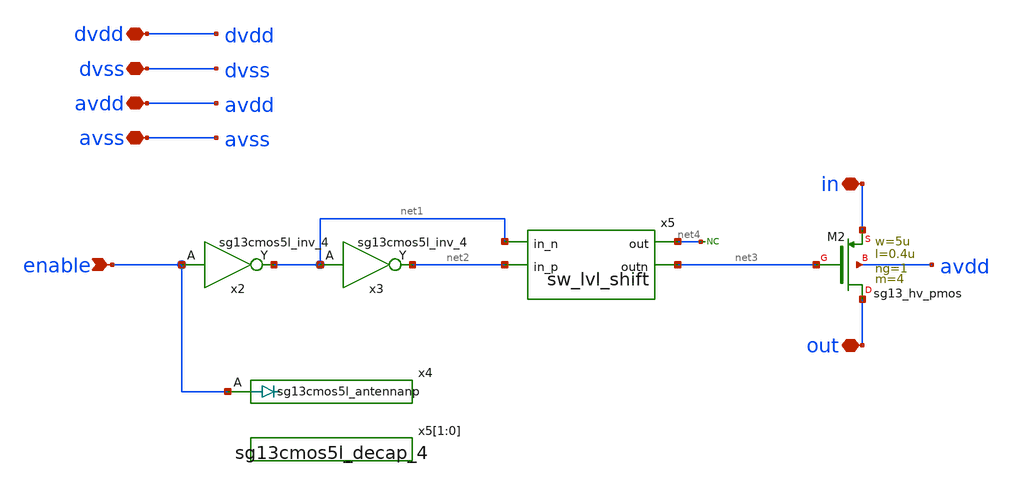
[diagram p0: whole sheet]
** sch_path: macros/ocd_analog_switches/schematic/xschem/analog_pswitch_small.sch
**.subckt analog_pswitch_small in out enable dvdd dvss avdd avss
*.iopin in
*.iopin out
*.ipin enable
*.iopin dvdd
*.iopin dvss
*.iopin avdd
*.iopin avss
XM2 out net3 in avdd sg13_hv_pmos w=5u l=0.4u ng=1 m=4 mm_ok=1
x2 net1 enable dvdd dvss sg13cmos5l_inv_4
x3 net2 net1 dvdd dvss sg13cmos5l_inv_4
x4 enable dvdd dvss sg13cmos5l_antennanp
x5[1] dvdd dvss sg13cmos5l_decap_4
x5[0] dvdd dvss sg13cmos5l_decap_4
x5 net2 net1 net4 net3 avdd avss sw_lvl_shift
* noconn #net4
**.ends

* expanding   symbol:  sw_lvl_shift.sym # of pins=4
** sym_path: macros/ocd_analog_switches/schematic/xschem/sw_lvl_shift.sym
** sch_path: macros/ocd_analog_switches/schematic/xschem/sw_lvl_shift.sch
.subckt sw_lvl_shift in_p in_n out outn avdd avss
*.ipin in_n
*.ipin in_p
*.opin out
*.opin outn
XM1 net1 in_p avss avss sg13_hv_nmos w=2u l=0.5u ng=1 m=1 mm_ok=1
XM2 net1 S1_N avdd avdd sg13_hv_pmos w=0.5u l=0.5u ng=1 m=1 mm_ok=1
XM3 S1_N in_n avss avss sg13_hv_nmos w=2u l=0.5u ng=1 m=1 mm_ok=1
XM4 S1_N net1 avdd avdd sg13_hv_pmos w=0.5u l=0.5u ng=1 m=1 mm_ok=1
XM5 outn S1_N avdd avdd sg13_hv_pmos w=2u l=0.5u ng=1 m=2 mm_ok=1
XM6 outn S1_N avss avss sg13_hv_nmos w=1u l=0.5u ng=1 m=2 mm_ok=1
XM7 out outn avdd avdd sg13_hv_pmos w=2u l=0.5u ng=1 m=2 mm_ok=1
XM8 out outn avss avss sg13_hv_nmos w=1u l=0.5u ng=1 m=2 mm_ok=1
.ends

.end
